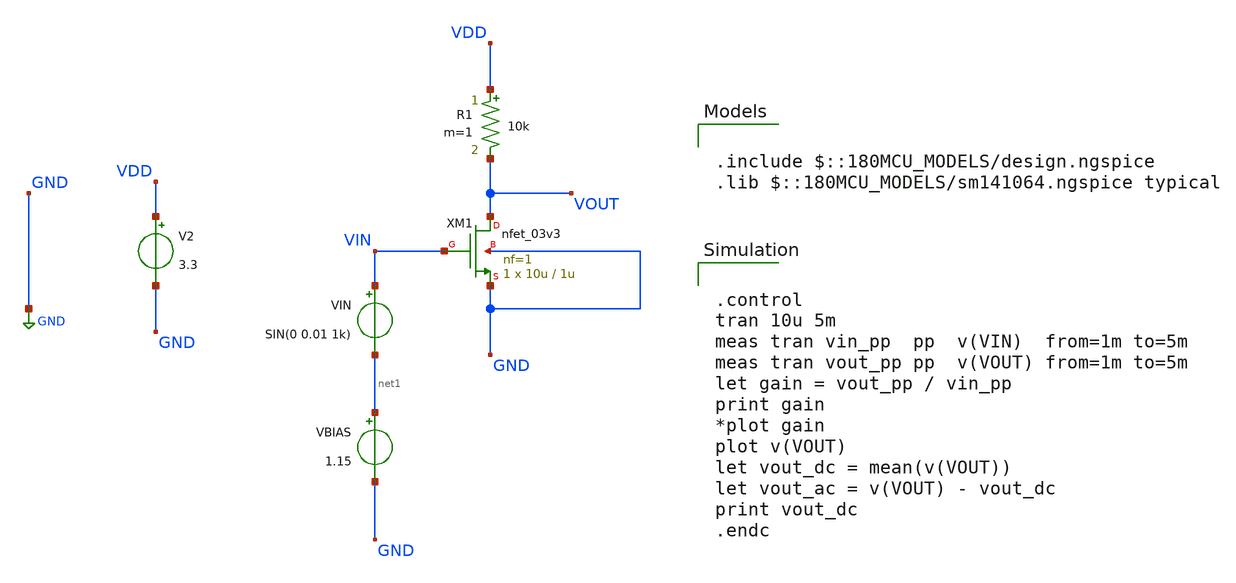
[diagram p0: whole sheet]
** sch_path: designs/sophiazhu/session_1/cs_res_load_amp.sch
**.subckt cs_res_load_amp
XM1 VOUT VIN GND GND nfet_03v3 L=1u W=10u nf=1 ad='int((nf+1)/2) * W/nf * 0.18u' as='int((nf+2)/2) * W/nf * 0.18u'
+ pd='2*int((nf+1)/2) * (W/nf + 0.18u)' ps='2*int((nf+2)/2) * (W/nf + 0.18u)' nrd='0.18u / W' nrs='0.18u / W'
+ sa=0 sb=0 sd=0 m=1
R1 VDD VOUT 10k m=1
V2 VDD GND 3.3
VBIAS net1 GND 1.15
VIN VIN net1 SIN(0 0.01 1k)
**** begin user architecture code


.control
tran 10u 5m
meas tran vin_pp  pp  v(VIN)  from=1m to=5m
meas tran vout_pp pp  v(VOUT) from=1m to=5m
let gain = vout_pp / vin_pp
print gain
*plot gain
plot v(VOUT)
let vout_dc = mean(v(VOUT))
let vout_ac = v(VOUT) - vout_dc
print vout_dc
.endc



.include $::180MCU_MODELS/design.ngspice
.lib $::180MCU_MODELS/sm141064.ngspice typical

**** end user architecture code
**.ends
.GLOBAL GND
.end
